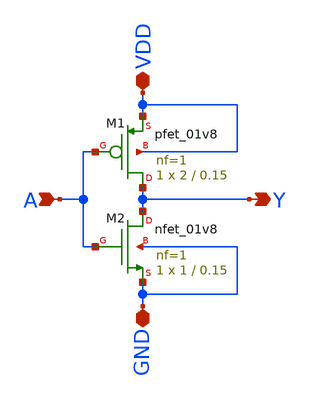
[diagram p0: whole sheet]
** sch_path: parity_ceker/schematic/not_std.sch
**.subckt not_std A Y VDD GND
*.ipin A
*.opin Y
*.iopin VDD
*.iopin GND
XM1 Y A VDD VDD sky130_fd_pr__pfet_01v8 L=0.15 W=2 nf=1 ad='int((1 + 1)/2) * 2 / 1 * 0.29' as='int((1 + 2)/2) * 2 / 1 * 0.29'
+ pd='2*int((1 + 1)/2) * (2 / 1 + 0.29)' ps='2*int((1 + 2)/2) * (2 / 1 + 0.29)' nrd='0.29 / 2 ' nrs='0.29 / 2 '
+ sa=0 sb=0 sd=0 mult=1 m=1
XM2 Y A GND GND sky130_fd_pr__nfet_01v8 L=0.15 W=1 nf=1 ad='int((1 + 1)/2) * 1 / 1 * 0.29' as='int((1 + 2)/2) * 1 / 1 * 0.29'
+ pd='2*int((1 + 1)/2) * (1 / 1 + 0.29)' ps='2*int((1 + 2)/2) * (1 / 1 + 0.29)' nrd='0.29 / 1 ' nrs='0.29 / 1 '
+ sa=0 sb=0 sd=0 mult=1 m=1
**.ends
.end
